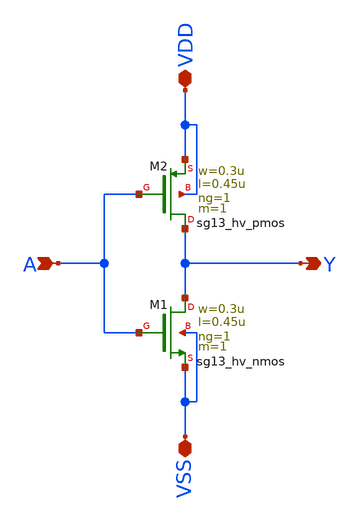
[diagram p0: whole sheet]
** sch_path: xschem/inverter.sch
**.subckt inverter A Y VDD VSS
*.ipin A
*.opin Y
*.iopin VDD
*.iopin VSS
XM1 Y A VSS VSS sg13_hv_nmos w=0.3u l=0.45u ng=1 m=1 mm_ok=1
XM2 Y A VDD VDD sg13_hv_pmos w=0.3u l=0.45u ng=1 m=1 mm_ok=1
**.ends
.end
